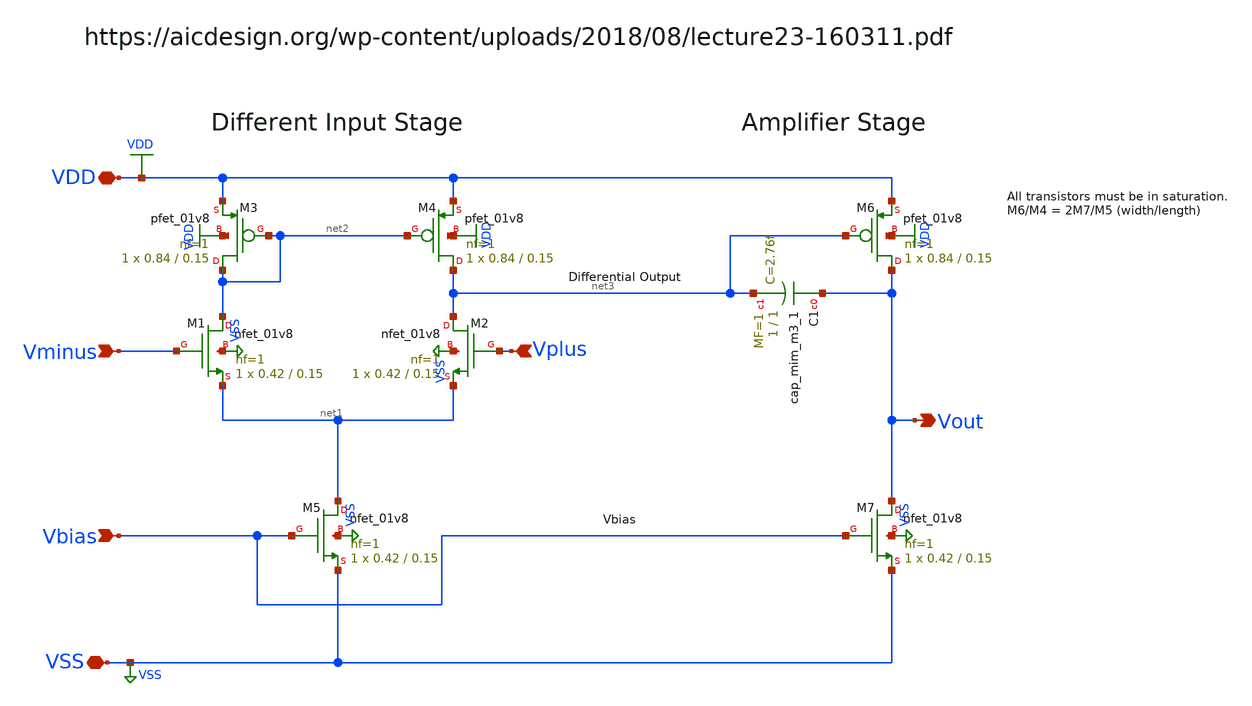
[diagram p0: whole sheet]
** sch_path: test/template/OpAmp.sch
**.subckt OpAmp Vplus Vminus VDD VSS Vbias Vout
*.ipin Vplus
*.ipin Vminus
*.iopin VDD
*.iopin VSS
*.ipin Vbias
*.opin Vout
XM1 net2 Vminus net1 VSS sky130_fd_pr__nfet_01v8 L=0.15 W=0.42 nf=1 ad='int((nf+1)/2) * W/nf * 0.29'
+ as='int((nf+2)/2) * W/nf * 0.29' pd='2*int((nf+1)/2) * (W/nf + 0.29)' ps='2*int((nf+2)/2) * (W/nf + 0.29)'
+ nrd='0.29 / W' nrs='0.29 / W' sa=0 sb=0 sd=0 mult=1 m=1
XM2 net3 Vplus net1 VSS sky130_fd_pr__nfet_01v8 L=0.15 W=0.42 nf=1 ad='int((nf+1)/2) * W/nf * 0.29' as='int((nf+2)/2) * W/nf * 0.29'
+ pd='2*int((nf+1)/2) * (W/nf + 0.29)' ps='2*int((nf+2)/2) * (W/nf + 0.29)' nrd='0.29 / W' nrs='0.29 / W'
+ sa=0 sb=0 sd=0 mult=1 m=1
XM3 net2 net2 VDD VDD sky130_fd_pr__pfet_01v8 L=0.15 W=0.84 nf=1 ad='int((nf+1)/2) * W/nf * 0.29' as='int((nf+2)/2) * W/nf * 0.29'
+ pd='2*int((nf+1)/2) * (W/nf + 0.29)' ps='2*int((nf+2)/2) * (W/nf + 0.29)' nrd='0.29 / W' nrs='0.29 / W'
+ sa=0 sb=0 sd=0 mult=1 m=1
XM4 net3 net2 VDD VDD sky130_fd_pr__pfet_01v8 L=0.15 W=0.84 nf=1 ad='int((nf+1)/2) * W/nf * 0.29' as='int((nf+2)/2) * W/nf * 0.29'
+ pd='2*int((nf+1)/2) * (W/nf + 0.29)' ps='2*int((nf+2)/2) * (W/nf + 0.29)' nrd='0.29 / W' nrs='0.29 / W'
+ sa=0 sb=0 sd=0 mult=1 m=1
XM5 net1 Vbias VSS VSS sky130_fd_pr__nfet_01v8 L=0.15 W=0.42 nf=1 ad='int((nf+1)/2) * W/nf * 0.29' as='int((nf+2)/2) * W/nf * 0.29'
+ pd='2*int((nf+1)/2) * (W/nf + 0.29)' ps='2*int((nf+2)/2) * (W/nf + 0.29)' nrd='0.29 / W' nrs='0.29 / W'
+ sa=0 sb=0 sd=0 mult=1 m=1
XM6 Vout net3 VDD VDD sky130_fd_pr__pfet_01v8 L=0.15 W=0.84 nf=1 ad='int((nf+1)/2) * W/nf * 0.29' as='int((nf+2)/2) * W/nf * 0.29'
+ pd='2*int((nf+1)/2) * (W/nf + 0.29)' ps='2*int((nf+2)/2) * (W/nf + 0.29)' nrd='0.29 / W' nrs='0.29 / W'
+ sa=0 sb=0 sd=0 mult=1 m=1
XC1 Vout net3 sky130_fd_pr__cap_mim_m3_1 W=1 L=1 MF=1 m=1
XM7 Vout Vbias VSS VSS sky130_fd_pr__nfet_01v8 L=0.15 W=0.42 nf=1 ad='int((nf+1)/2) * W/nf * 0.29' as='int((nf+2)/2) * W/nf * 0.29'
+ pd='2*int((nf+1)/2) * (W/nf + 0.29)' ps='2*int((nf+2)/2) * (W/nf + 0.29)' nrd='0.29 / W' nrs='0.29 / W'
+ sa=0 sb=0 sd=0 mult=1 m=1
**.ends
.GLOBAL VDD
.GLOBAL VSS
.end
